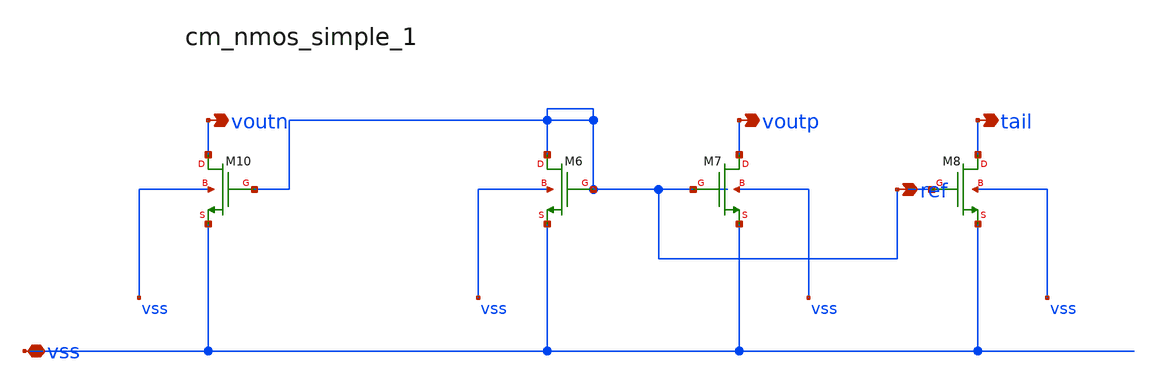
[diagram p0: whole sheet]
** sch_path: analog-db/raw/amp_029_two_stage_miller_comp/hier/blocks/cm_nmos_simple_1.sch
**.subckt cm_nmos_simple_1 vss voutn ref voutp tail
*.iopin vss
*.opin voutn
*.opin ref
*.opin voutp
*.opin tail
XM10 voutn ref vss vss sg13_lv_nmos w=x_dut_xm10_w l=x_dut_xm10_l ng=1 m=x_dut_xm10_m
XM6 ref ref vss vss sg13_lv_nmos w=x_dut_xm6_w l=x_dut_xm6_l ng=1 m=x_dut_xm6_m
XM7 voutp ref vss vss sg13_lv_nmos w=x_dut_xm7_w l=x_dut_xm7_l ng=1 m=x_dut_xm7_m
XM8 tail ref vss vss sg13_lv_nmos w=x_dut_xm8_w l=x_dut_xm8_l ng=1 m=x_dut_xm8_m
**.ends
.end
